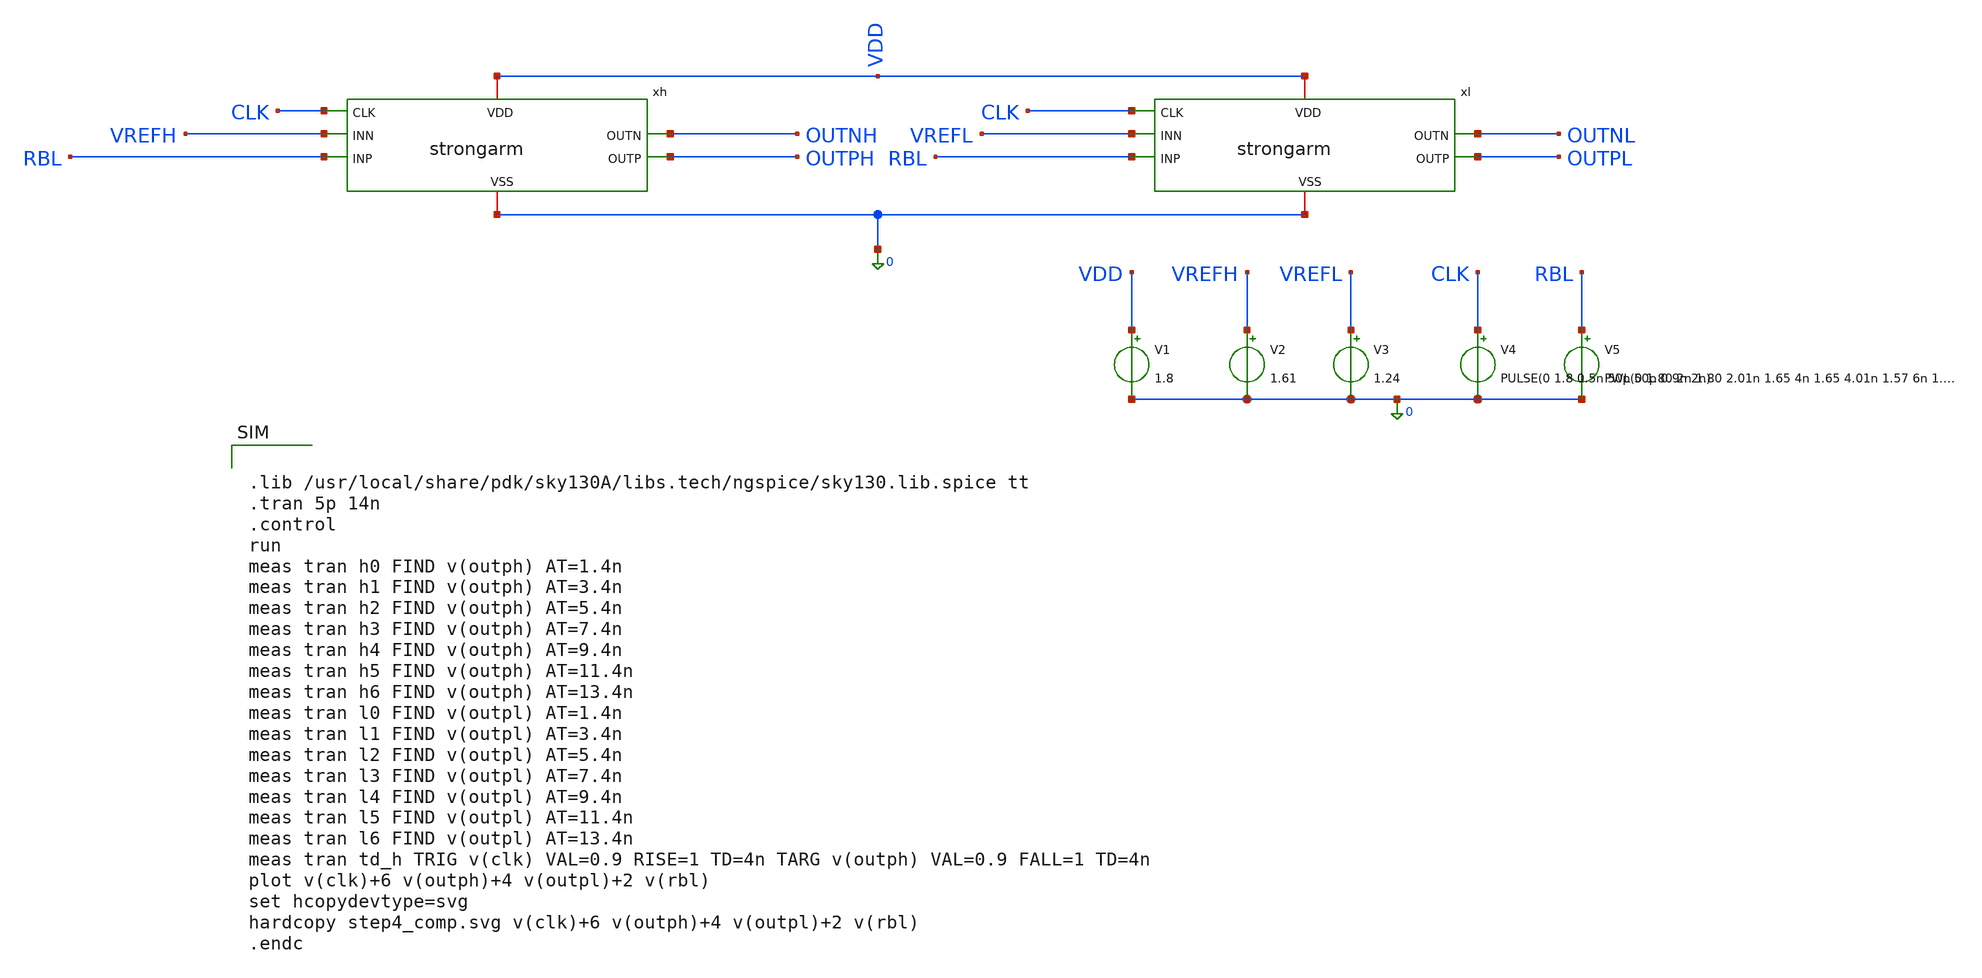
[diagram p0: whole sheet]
** sch_path: schematics/strongarm_tb.sch
**.subckt strongarm_tb
xh VDD CLK OUTNH OUTPH VREFH RBL 0 strongarm
xl VDD CLK OUTNL OUTPL VREFL RBL 0 strongarm
V1 VDD 0 1.8
V2 VREFH 0 1.61
V3 VREFL 0 1.24
V4 CLK 0 PULSE(0 1.8 0.5n 50p 50p 0.9n 2n)
V5 RBL 0 PWL(0 1.80 2n 1.80 2.01n 1.65 4n 1.65 4.01n 1.57 6n 1.57 6.01n 1.42 8n 1.42 8.01n 1.28 10n
+ 1.28 10.01n 1.20 12n 1.20 12.01n 1.05 14n 1.05)
**** begin user architecture code


.lib /usr/local/share/pdk/sky130A/libs.tech/ngspice/sky130.lib.spice tt
.tran 5p 14n
.control
run
meas tran h0 FIND v(outph) AT=1.4n
meas tran h1 FIND v(outph) AT=3.4n
meas tran h2 FIND v(outph) AT=5.4n
meas tran h3 FIND v(outph) AT=7.4n
meas tran h4 FIND v(outph) AT=9.4n
meas tran h5 FIND v(outph) AT=11.4n
meas tran h6 FIND v(outph) AT=13.4n
meas tran l0 FIND v(outpl) AT=1.4n
meas tran l1 FIND v(outpl) AT=3.4n
meas tran l2 FIND v(outpl) AT=5.4n
meas tran l3 FIND v(outpl) AT=7.4n
meas tran l4 FIND v(outpl) AT=9.4n
meas tran l5 FIND v(outpl) AT=11.4n
meas tran l6 FIND v(outpl) AT=13.4n
meas tran td_h TRIG v(clk) VAL=0.9 RISE=1 TD=4n TARG v(outph) VAL=0.9 FALL=1 TD=4n
plot v(clk)+6 v(outph)+4 v(outpl)+2 v(rbl)
set hcopydevtype=svg
hardcopy step4_comp.svg v(clk)+6 v(outph)+4 v(outpl)+2 v(rbl)
.endc


**** end user architecture code
**.ends
.end
